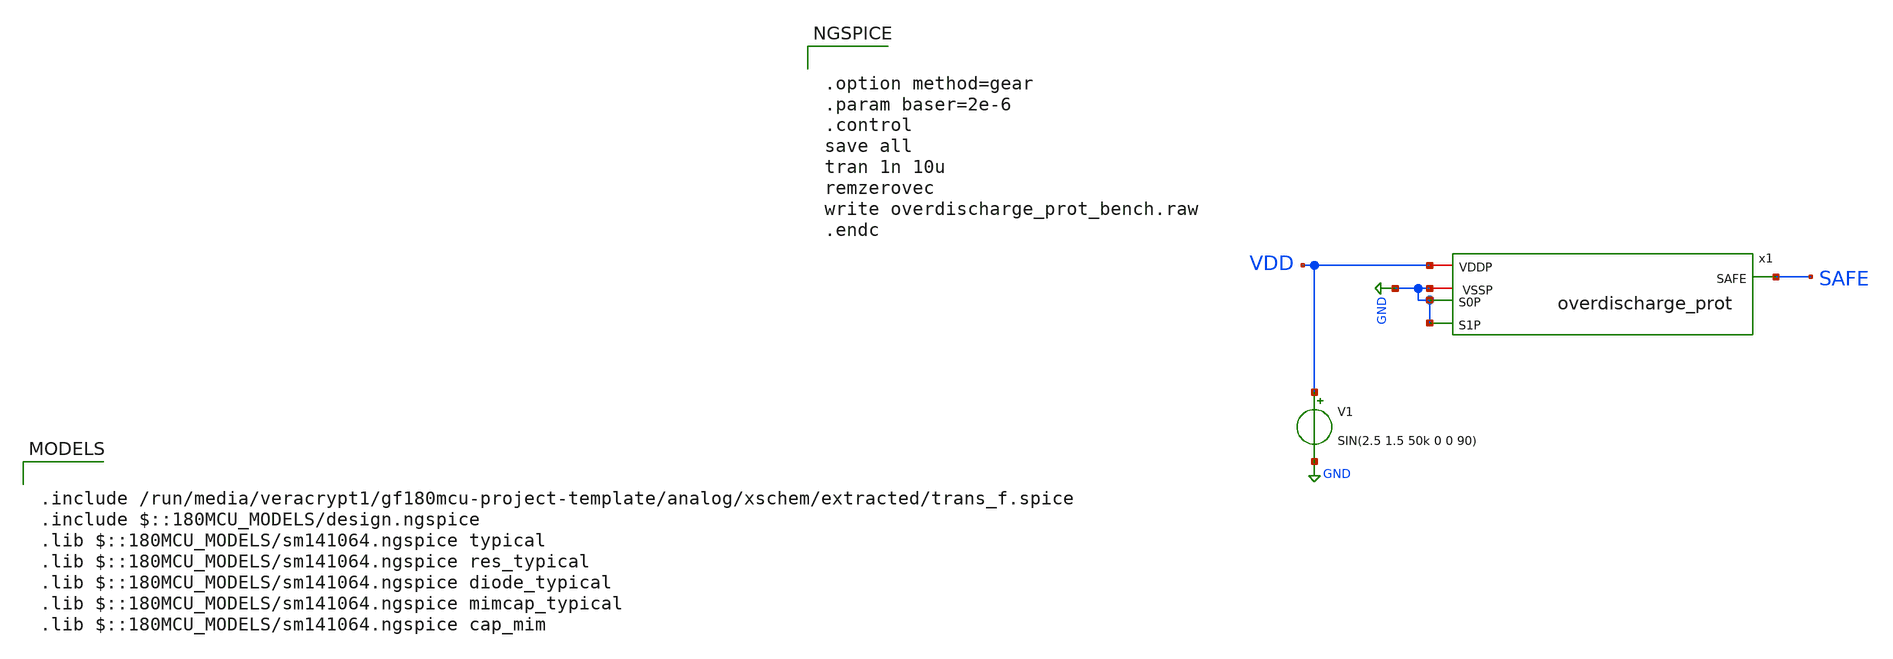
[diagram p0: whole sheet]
** sch_path: analog/xschem/overdischarge_prot_bench.sch
**.subckt overdischarge_prot_bench
x1 GND GND SAFE VDD GND overdischarge_prot
V1 VDD GND SIN(2.5 1.5 50k 0 0 90)
**** begin user architecture code


.option method=gear
.param baser=2e-6
.control
save all
tran 1n 10u
remzerovec
write overdischarge_prot_bench.raw
.endc



.include /run/media/veracrypt1/gf180mcu-project-template/analog/xschem/extracted/trans_f.spice
.include $::180MCU_MODELS/design.ngspice
.lib $::180MCU_MODELS/sm141064.ngspice typical
.lib $::180MCU_MODELS/sm141064.ngspice res_typical
.lib $::180MCU_MODELS/sm141064.ngspice diode_typical
.lib $::180MCU_MODELS/sm141064.ngspice mimcap_typical
.lib $::180MCU_MODELS/sm141064.ngspice cap_mim

**** end user architecture code
**.ends

* expanding   symbol:  overdischarge_prot.sym # of pins=5
** sym_path: analog/xschem/overdischarge_prot.sym
** sch_path: analog/xschem/overdischarge_prot.sch
.subckt overdischarge_prot S0P S1P SAFE VDDP VSSP
*.iopin VDDP
*.iopin VSSP
*.opin SAFE
*.ipin S0P
*.ipin S1P
x1 VDDP TRIP PLUS MINUS VSSP comparator
x2 VDDP PLUS VSSP voltage_ref
XM1 VSSP TRIP net1 VSSP nfet_06v0 L=0.70u W=2u nf=1 ad='int((nf+1)/2) * W/nf * 0.18u' as='int((nf+2)/2) * W/nf * 0.18u'
+ pd='2*int((nf+1)/2) * (W/nf + 0.18u)' ps='2*int((nf+2)/2) * (W/nf + 0.18u)' nrd='0.18u / W' nrs='0.18u / W'
+ sa=0 sb=0 sd=0 m=1
XR1 VSSP net1 VSSP ppolyf_u_1k_6p0 r_width=1e-6 r_length=2e-6 m=1
XR2 net1 MINUS VSSP ppolyf_u_1k_6p0 r_width=1e-6 r_length=8e-6 m=1
XR3 MINUS net3 VSSP ppolyf_u_1k_6p0 r_width=1e-6 r_length=1.7e-5 m=1
XM2 SAFE TRIP VSSP VSSP nfet_06v0 L=0.70u W=8u nf=1 ad='int((nf+1)/2) * W/nf * 0.18u' as='int((nf+2)/2) * W/nf * 0.18u'
+ pd='2*int((nf+1)/2) * (W/nf + 0.18u)' ps='2*int((nf+2)/2) * (W/nf + 0.18u)' nrd='0.18u / W' nrs='0.18u / W'
+ sa=0 sb=0 sd=0 m=1
XM3 SAFE TRIP VDDP VDDP pfet_06v0 L=0.55u W=8u nf=1 ad='int((nf+1)/2) * W/nf * 0.18u' as='int((nf+2)/2) * W/nf * 0.18u'
+ pd='2*int((nf+1)/2) * (W/nf + 0.18u)' ps='2*int((nf+2)/2) * (W/nf + 0.18u)' nrd='0.18u / W' nrs='0.18u / W'
+ sa=0 sb=0 sd=0 m=1
XM4 S0Pn S0P VDDP VDDP pfet_06v0 L=0.55u W=1u nf=1 ad='int((nf+1)/2) * W/nf * 0.18u' as='int((nf+2)/2) * W/nf * 0.18u'
+ pd='2*int((nf+1)/2) * (W/nf + 0.18u)' ps='2*int((nf+2)/2) * (W/nf + 0.18u)' nrd='0.18u / W' nrs='0.18u / W'
+ sa=0 sb=0 sd=0 m=1
XM5 S0Pn S0P VSSP VSSP nfet_06v0 L=0.70u W=1u nf=1 ad='int((nf+1)/2) * W/nf * 0.18u' as='int((nf+2)/2) * W/nf * 0.18u'
+ pd='2*int((nf+1)/2) * (W/nf + 0.18u)' ps='2*int((nf+2)/2) * (W/nf + 0.18u)' nrd='0.18u / W' nrs='0.18u / W'
+ sa=0 sb=0 sd=0 m=1
XM6 S1Pn S1P VDDP VDDP pfet_06v0 L=0.55u W=1u nf=1 ad='int((nf+1)/2) * W/nf * 0.18u' as='int((nf+2)/2) * W/nf * 0.18u'
+ pd='2*int((nf+1)/2) * (W/nf + 0.18u)' ps='2*int((nf+2)/2) * (W/nf + 0.18u)' nrd='0.18u / W' nrs='0.18u / W'
+ sa=0 sb=0 sd=0 m=1
XM7 S1Pn S1P VSSP VSSP nfet_06v0 L=0.70u W=1u nf=1 ad='int((nf+1)/2) * W/nf * 0.18u' as='int((nf+2)/2) * W/nf * 0.18u'
+ pd='2*int((nf+1)/2) * (W/nf + 0.18u)' ps='2*int((nf+2)/2) * (W/nf + 0.18u)' nrd='0.18u / W' nrs='0.18u / W'
+ sa=0 sb=0 sd=0 m=1
XR4 MINUS net5 VSSP ppolyf_u_1k_6p0 r_width=1e-6 r_length=2.97e-5 m=1
XR6 MINUS net2 VSSP ppolyf_u_1k_6p0 r_width=1e-6 r_length=1.9e-5 m=1
XM10 net2 S0P net4 VDDP pfet_06v0 L=0.55u W=8u nf=1 ad='int((nf+1)/2) * W/nf * 0.18u' as='int((nf+2)/2) * W/nf * 0.18u'
+ pd='2*int((nf+1)/2) * (W/nf + 0.18u)' ps='2*int((nf+2)/2) * (W/nf + 0.18u)' nrd='0.18u / W' nrs='0.18u / W'
+ sa=0 sb=0 sd=0 m=1
XM11 net3 S0Pn net4 VDDP pfet_06v0 L=0.55u W=8u nf=1 ad='int((nf+1)/2) * W/nf * 0.18u' as='int((nf+2)/2) * W/nf * 0.18u'
+ pd='2*int((nf+1)/2) * (W/nf + 0.18u)' ps='2*int((nf+2)/2) * (W/nf + 0.18u)' nrd='0.18u / W' nrs='0.18u / W'
+ sa=0 sb=0 sd=0 m=1
XM12 net5 S1P VDDP VDDP pfet_06v0 L=0.55u W=8u nf=1 ad='int((nf+1)/2) * W/nf * 0.18u' as='int((nf+2)/2) * W/nf * 0.18u'
+ pd='2*int((nf+1)/2) * (W/nf + 0.18u)' ps='2*int((nf+2)/2) * (W/nf + 0.18u)' nrd='0.18u / W' nrs='0.18u / W'
+ sa=0 sb=0 sd=0 m=1
XM14 net4 S1Pn VDDP VDDP pfet_06v0 L=0.55u W=8u nf=1 ad='int((nf+1)/2) * W/nf * 0.18u' as='int((nf+2)/2) * W/nf * 0.18u'
+ pd='2*int((nf+1)/2) * (W/nf + 0.18u)' ps='2*int((nf+2)/2) * (W/nf + 0.18u)' nrd='0.18u / W' nrs='0.18u / W'
+ sa=0 sb=0 sd=0 m=1
.ends


* expanding   symbol:  comparator.sym # of pins=5
** sym_path: analog/xschem/comparator.sym
** sch_path: analog/xschem/comparator.sch
.subckt comparator VDD OUT PLUS MINUS VSS
*.ipin VDD
*.ipin PLUS
*.ipin VSS
*.opin OUT
*.ipin MINUS
XM3 i1 net1 VDD VDD pfet_06v0 L=1.1u W=3u nf=1 ad='int((nf+1)/2) * W/nf * 0.18u' as='int((nf+2)/2) * W/nf * 0.18u'
+ pd='2*int((nf+1)/2) * (W/nf + 0.18u)' ps='2*int((nf+2)/2) * (W/nf + 0.18u)' nrd='0.18u / W' nrs='0.18u / W'
+ sa=0 sb=0 sd=0 m=1
XM4 net2 MINUS VDD VDD pfet_06v0 L=1.1u W=3u nf=1 ad='int((nf+1)/2) * W/nf * 0.18u' as='int((nf+2)/2) * W/nf * 0.18u'
+ pd='2*int((nf+1)/2) * (W/nf + 0.18u)' ps='2*int((nf+2)/2) * (W/nf + 0.18u)' nrd='0.18u / W' nrs='0.18u / W'
+ sa=0 sb=0 sd=0 m=1
XM5 net1 PLUS VDD VDD pfet_06v0 L=1.1u W=3u nf=1 ad='int((nf+1)/2) * W/nf * 0.18u' as='int((nf+2)/2) * W/nf * 0.18u'
+ pd='2*int((nf+1)/2) * (W/nf + 0.18u)' ps='2*int((nf+2)/2) * (W/nf + 0.18u)' nrd='0.18u / W' nrs='0.18u / W'
+ sa=0 sb=0 sd=0 m=1
XM6 net2 net2 VSS VSS nfet_06v0 L=1.4u W=3u nf=1 ad='int((nf+1)/2) * W/nf * 0.18u' as='int((nf+2)/2) * W/nf * 0.18u'
+ pd='2*int((nf+1)/2) * (W/nf + 0.18u)' ps='2*int((nf+2)/2) * (W/nf + 0.18u)' nrd='0.18u / W' nrs='0.18u / W'
+ sa=0 sb=0 sd=0 m=1
XM7 net1 net2 VSS VSS nfet_06v0 L=1.4u W=3u nf=1 ad='int((nf+1)/2) * W/nf * 0.18u' as='int((nf+2)/2) * W/nf * 0.18u'
+ pd='2*int((nf+1)/2) * (W/nf + 0.18u)' ps='2*int((nf+2)/2) * (W/nf + 0.18u)' nrd='0.18u / W' nrs='0.18u / W'
+ sa=0 sb=0 sd=0 m=1
XM8 i1 net1 VSS VSS nfet_06v0 L=1.4u W=3u nf=1 ad='int((nf+1)/2) * W/nf * 0.18u' as='int((nf+2)/2) * W/nf * 0.18u'
+ pd='2*int((nf+1)/2) * (W/nf + 0.18u)' ps='2*int((nf+2)/2) * (W/nf + 0.18u)' nrd='0.18u / W' nrs='0.18u / W'
+ sa=0 sb=0 sd=0 m=1
x1 VDD i1 net3 VSS schmitt
XM9 OUT net3 VDD VDD pfet_06v0 L=0.55u W=24u nf=3 ad='int((nf+1)/2) * W/nf * 0.18u' as='int((nf+2)/2) * W/nf * 0.18u'
+ pd='2*int((nf+1)/2) * (W/nf + 0.18u)' ps='2*int((nf+2)/2) * (W/nf + 0.18u)' nrd='0.18u / W' nrs='0.18u / W'
+ sa=0 sb=0 sd=0 m=1
XM10 OUT net3 VSS VSS nfet_06v0 L=0.70u W=24u nf=3 ad='int((nf+1)/2) * W/nf * 0.18u' as='int((nf+2)/2) * W/nf * 0.18u'
+ pd='2*int((nf+1)/2) * (W/nf + 0.18u)' ps='2*int((nf+2)/2) * (W/nf + 0.18u)' nrd='0.18u / W' nrs='0.18u / W'
+ sa=0 sb=0 sd=0 m=1
.ends


* expanding   symbol:  voltage_ref.sym # of pins=3
** sym_path: analog/xschem/voltage_ref.sym
** sch_path: analog/xschem/voltage_ref.sch
.subckt voltage_ref VDD VREF VSS
*.ipin VDD
*.ipin VSS
*.opin VREF
XM1 net1 net1 VDD VDD pfet_06v0 L=5u W=10u nf=1 ad='int((nf+1)/2) * W/nf * 0.18u' as='int((nf+2)/2) * W/nf * 0.18u'
+ pd='2*int((nf+1)/2) * (W/nf + 0.18u)' ps='2*int((nf+2)/2) * (W/nf + 0.18u)' nrd='0.18u / W' nrs='0.18u / W'
+ sa=0 sb=0 sd=0 m=1
XM2 net2 net1 VDD VDD pfet_06v0 L=5u W=10u nf=1 ad='int((nf+1)/2) * W/nf * 0.18u' as='int((nf+2)/2) * W/nf * 0.18u'
+ pd='2*int((nf+1)/2) * (W/nf + 0.18u)' ps='2*int((nf+2)/2) * (W/nf + 0.18u)' nrd='0.18u / W' nrs='0.18u / W'
+ sa=0 sb=0 sd=0 m=1
XM3 VREF net1 VDD VDD pfet_06v0 L=5u W=10u nf=1 ad='int((nf+1)/2) * W/nf * 0.18u' as='int((nf+2)/2) * W/nf * 0.18u'
+ pd='2*int((nf+1)/2) * (W/nf + 0.18u)' ps='2*int((nf+2)/2) * (W/nf + 0.18u)' nrd='0.18u / W' nrs='0.18u / W'
+ sa=0 sb=0 sd=0 m=1
XM4 net1 net2 net3 VSS nfet_06v0 L=2.5u W=10u nf=1 ad='int((nf+1)/2) * W/nf * 0.18u' as='int((nf+2)/2) * W/nf * 0.18u'
+ pd='2*int((nf+1)/2) * (W/nf + 0.18u)' ps='2*int((nf+2)/2) * (W/nf + 0.18u)' nrd='0.18u / W' nrs='0.18u / W'
+ sa=0 sb=0 sd=0 m=1
XM5 net2 net2 net5 VSS nfet_06v0 L=2.5u W=10u nf=1 ad='int((nf+1)/2) * W/nf * 0.18u' as='int((nf+2)/2) * W/nf * 0.18u'
+ pd='2*int((nf+1)/2) * (W/nf + 0.18u)' ps='2*int((nf+2)/2) * (W/nf + 0.18u)' nrd='0.18u / W' nrs='0.18u / W'
+ sa=0 sb=0 sd=0 m=1
XR1 net4 net3 VSS ppolyf_u_1k_6p0 r_width=1e-6 r_length=5e-6 m=1
XR2 net6 VREF VSS ppolyf_u_1k_6p0 r_width=1e-6 r_length=5e-6 m=1
D3 net6 VSS diode_pd2nw_06v0 area='5u * 1u ' pj='2*5u + 2*1u ' m=1
D1 net5 VSS diode_pd2nw_06v0 area='5u * 1u ' pj='2*5u + 2*1u ' m=1
D2 net4 VSS diode_pd2nw_06v0 area='5u * 1u ' pj='2*5u + 2*1u ' m=1
.ends


* expanding   symbol:  schmitt.sym # of pins=4
** sym_path: analog/xschem/schmitt.sym
** sch_path: analog/xschem/schmitt.sch
.subckt schmitt VDD A Y VSS
*.ipin VDD
*.ipin VSS
*.ipin A
*.opin Y
XM1 net1 A VDD VDD pfet_06v0 L=0.55u W=4u nf=1 ad='int((nf+1)/2) * W/nf * 0.18u' as='int((nf+2)/2) * W/nf * 0.18u'
+ pd='2*int((nf+1)/2) * (W/nf + 0.18u)' ps='2*int((nf+2)/2) * (W/nf + 0.18u)' nrd='0.18u / W' nrs='0.18u / W'
+ sa=0 sb=0 sd=0 m=1
XM2 Y A net1 VDD pfet_06v0 L=0.55u W=4u nf=1 ad='int((nf+1)/2) * W/nf * 0.18u' as='int((nf+2)/2) * W/nf * 0.18u'
+ pd='2*int((nf+1)/2) * (W/nf + 0.18u)' ps='2*int((nf+2)/2) * (W/nf + 0.18u)' nrd='0.18u / W' nrs='0.18u / W'
+ sa=0 sb=0 sd=0 m=1
XM3 Y A net2 VSS nfet_06v0 L=0.70u W=4u nf=1 ad='int((nf+1)/2) * W/nf * 0.18u' as='int((nf+2)/2) * W/nf * 0.18u'
+ pd='2*int((nf+1)/2) * (W/nf + 0.18u)' ps='2*int((nf+2)/2) * (W/nf + 0.18u)' nrd='0.18u / W' nrs='0.18u / W'
+ sa=0 sb=0 sd=0 m=1
XM4 net2 A VSS VSS nfet_06v0 L=0.70u W=4u nf=1 ad='int((nf+1)/2) * W/nf * 0.18u' as='int((nf+2)/2) * W/nf * 0.18u'
+ pd='2*int((nf+1)/2) * (W/nf + 0.18u)' ps='2*int((nf+2)/2) * (W/nf + 0.18u)' nrd='0.18u / W' nrs='0.18u / W'
+ sa=0 sb=0 sd=0 m=1
XM5 VSS Y net1 VDD pfet_06v0 L=0.55u W=2u nf=1 ad='int((nf+1)/2) * W/nf * 0.18u' as='int((nf+2)/2) * W/nf * 0.18u'
+ pd='2*int((nf+1)/2) * (W/nf + 0.18u)' ps='2*int((nf+2)/2) * (W/nf + 0.18u)' nrd='0.18u / W' nrs='0.18u / W'
+ sa=0 sb=0 sd=0 m=1
XM6 VDD Y net2 VSS nfet_06v0 L=0.70u W=2u nf=1 ad='int((nf+1)/2) * W/nf * 0.18u' as='int((nf+2)/2) * W/nf * 0.18u'
+ pd='2*int((nf+1)/2) * (W/nf + 0.18u)' ps='2*int((nf+2)/2) * (W/nf + 0.18u)' nrd='0.18u / W' nrs='0.18u / W'
+ sa=0 sb=0 sd=0 m=1
.ends

.GLOBAL GND
.end
